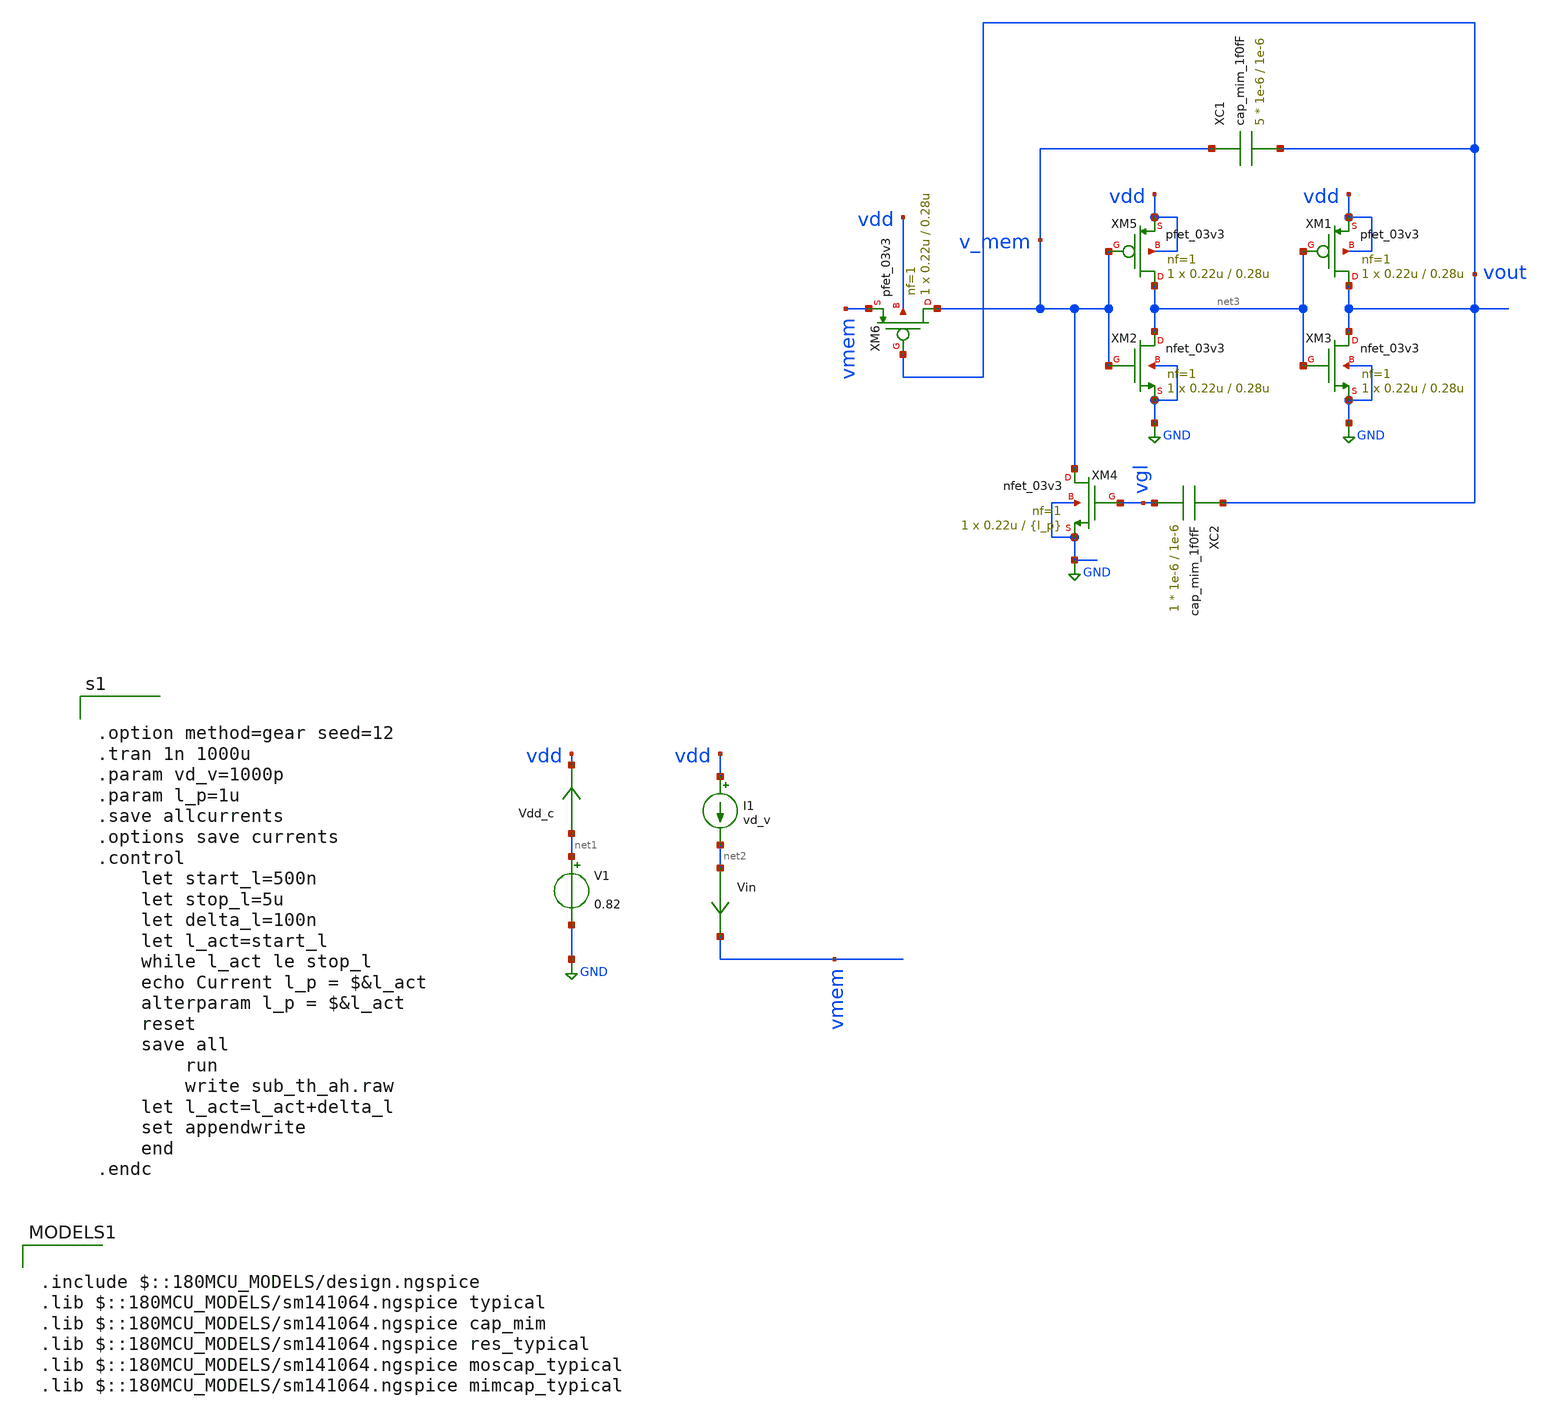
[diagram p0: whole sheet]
** sch_path: tst/AH_neuron_size.sch
**.subckt AH_neuron_size
V1 net1 GND 0.82
Vdd_c net1 vdd 0
.save i(vdd_c)
Vin net2 vmem 0
.save i(vin)
I1 vdd net2 vd_v
XM5 net3 v_mem vdd vdd pfet_03v3 L=0.28u W=0.22u nf=1 ad='int((nf+1)/2) * W/nf * 0.18u' as='int((nf+2)/2) * W/nf * 0.18u'
+ pd='2*int((nf+1)/2) * (W/nf + 0.18u)' ps='2*int((nf+2)/2) * (W/nf + 0.18u)' nrd='0.18u / W' nrs='0.18u / W'
+ sa=0 sb=0 sd=0 m=1
XM1 vout net3 vdd vdd pfet_03v3 L=0.28u W=0.22u nf=1 ad='int((nf+1)/2) * W/nf * 0.18u' as='int((nf+2)/2) * W/nf * 0.18u'
+ pd='2*int((nf+1)/2) * (W/nf + 0.18u)' ps='2*int((nf+2)/2) * (W/nf + 0.18u)' nrd='0.18u / W' nrs='0.18u / W'
+ sa=0 sb=0 sd=0 m=1
XM2 net3 v_mem GND GND nfet_03v3 L=0.28u W=0.22u nf=1 ad='int((nf+1)/2) * W/nf * 0.18u' as='int((nf+2)/2) * W/nf * 0.18u'
+ pd='2*int((nf+1)/2) * (W/nf + 0.18u)' ps='2*int((nf+2)/2) * (W/nf + 0.18u)' nrd='0.18u / W' nrs='0.18u / W'
+ sa=0 sb=0 sd=0 m=1
XM3 vout net3 GND GND nfet_03v3 L=0.28u W=0.22u nf=1 ad='int((nf+1)/2) * W/nf * 0.18u' as='int((nf+2)/2) * W/nf * 0.18u'
+ pd='2*int((nf+1)/2) * (W/nf + 0.18u)' ps='2*int((nf+2)/2) * (W/nf + 0.18u)' nrd='0.18u / W' nrs='0.18u / W'
+ sa=0 sb=0 sd=0 m=1
XC1 v_mem vout cap_mim_1f0fF c_width=1e-6 c_length=1e-6 m=5
XC2 vout vgl cap_mim_1f0fF c_width=1e-6 c_length=1e-6 m=1
XM6 v_mem vout vmem vdd pfet_03v3 L=0.28u W=0.22u nf=1 ad='int((nf+1)/2) * W/nf * 0.18u' as='int((nf+2)/2) * W/nf * 0.18u'
+ pd='2*int((nf+1)/2) * (W/nf + 0.18u)' ps='2*int((nf+2)/2) * (W/nf + 0.18u)' nrd='0.18u / W' nrs='0.18u / W'
+ sa=0 sb=0 sd=0 m=1
XM4 v_mem vgl GND GND nfet_03v3 L={l_p} W=0.22u nf=1 ad='int((nf+1)/2) * W/nf * 0.18u' as='int((nf+2)/2) * W/nf * 0.18u'
+ pd='2*int((nf+1)/2) * (W/nf + 0.18u)' ps='2*int((nf+2)/2) * (W/nf + 0.18u)' nrd='0.18u / W' nrs='0.18u / W'
+ sa=0 sb=0 sd=0 m=1
**** begin user architecture code


.option method=gear seed=12
.tran 1n 1000u
.param vd_v=1000p
.param l_p=1u
.save allcurrents
.options save currents
.control
    let start_l=500n
    let stop_l=5u
    let delta_l=100n
    let l_act=start_l
    while l_act le stop_l
	echo Current l_p = $&l_act
	alterparam l_p = $&l_act
	reset
	save all
        run
        write sub_th_ah.raw
	let l_act=l_act+delta_l
	set appendwrite
    end
.endc



.include $::180MCU_MODELS/design.ngspice
.lib $::180MCU_MODELS/sm141064.ngspice typical
.lib $::180MCU_MODELS/sm141064.ngspice cap_mim
.lib $::180MCU_MODELS/sm141064.ngspice res_typical
.lib $::180MCU_MODELS/sm141064.ngspice moscap_typical
.lib $::180MCU_MODELS/sm141064.ngspice mimcap_typical

**** end user architecture code
**.ends
.GLOBAL GND
.end
